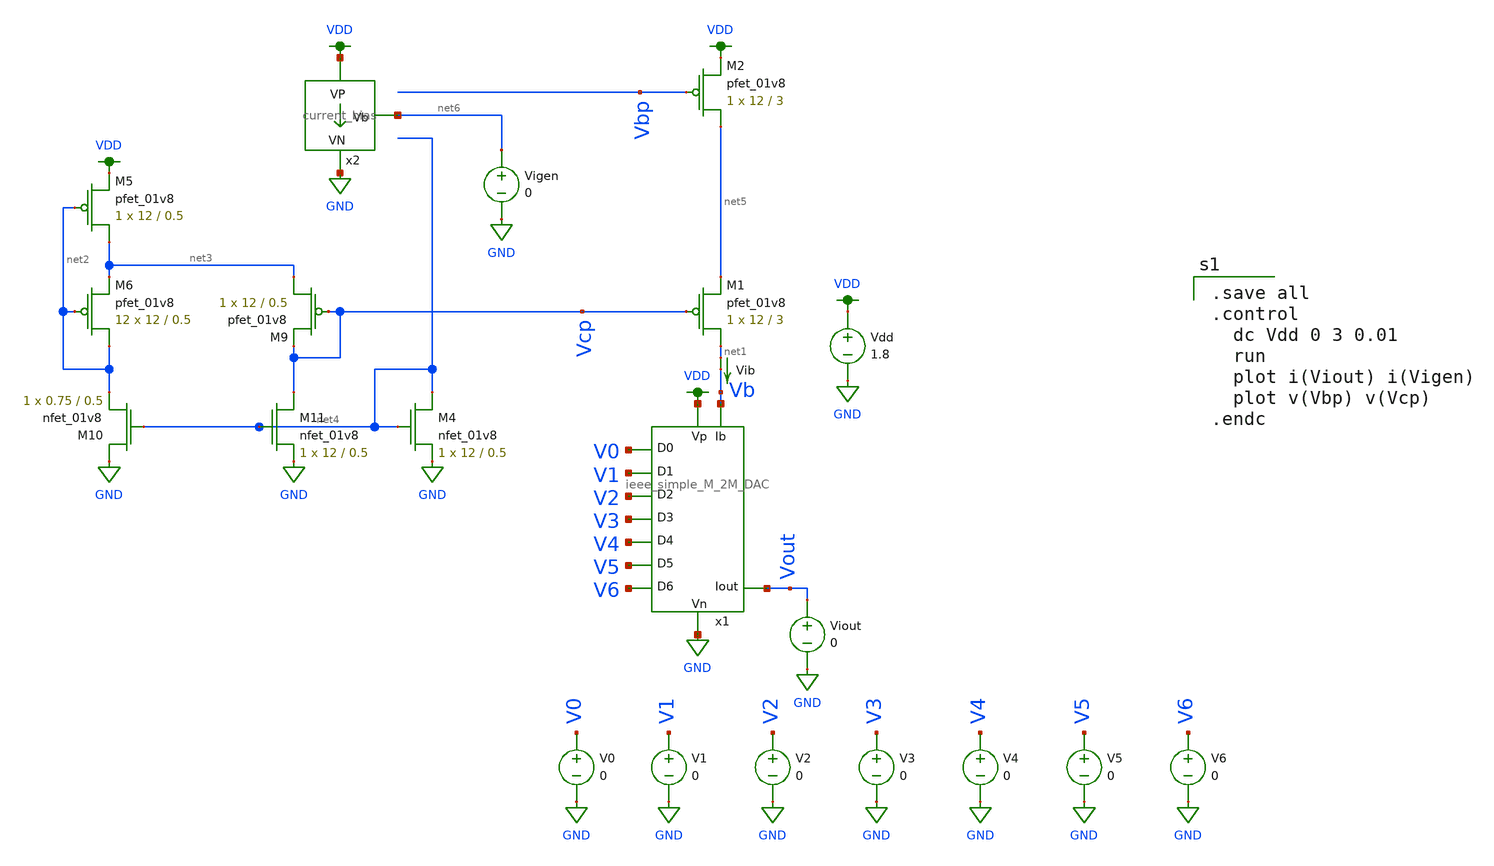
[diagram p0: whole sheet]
** sch_path: schematics/ieee DAC/characterization/bias_gen_with_cascode_and_vcn_generator.sch
**.subckt bias_gen_with_cascode_and_vcn_generator
Vdd VDD GND 1.8
V1 V1 GND 0
V2 V2 GND 0
V3 V3 GND 0
V4 V4 GND 0
V5 V5 GND 0
V6 V6 GND 0
V0 V0 GND 0
Viout Vout GND 0
Vib net1 Vb 0
.save i(vib)
x1 VDD Vout GND V1 V0 V2 V3 V4 V5 V6 Vb ieee_simple_M_2M_DAC
XM1 net1 Vcp net5 VDD sky130_fd_pr__pfet_01v8 L=3 W=12 nf=1 ad='int((nf+1)/2) * W/nf * 0.29' as='int((nf+2)/2) * W/nf * 0.29'
+ pd='2*int((nf+1)/2) * (W/nf + 0.29)' ps='2*int((nf+2)/2) * (W/nf + 0.29)' nrd='0.29 / W' nrs='0.29 / W'
+ sa=0 sb=0 sd=0 mult=1 m=1
XM5 net3 net2 VDD VDD sky130_fd_pr__pfet_01v8 L=0.5 W=12 nf=1 ad='int((nf+1)/2) * W/nf * 0.29' as='int((nf+2)/2) * W/nf * 0.29'
+ pd='2*int((nf+1)/2) * (W/nf + 0.29)' ps='2*int((nf+2)/2) * (W/nf + 0.29)' nrd='0.29 / W' nrs='0.29 / W'
+ sa=0 sb=0 sd=0 mult=1 m=1
XM6 net2 net2 net3 VDD sky130_fd_pr__pfet_01v8 L=0.5 W=12 nf=1 ad='int((nf+1)/2) * W/nf * 0.29' as='int((nf+2)/2) * W/nf * 0.29'
+ pd='2*int((nf+1)/2) * (W/nf + 0.29)' ps='2*int((nf+2)/2) * (W/nf + 0.29)' nrd='0.29 / W' nrs='0.29 / W'
+ sa=0 sb=0 sd=0 mult=12 m=12
XM9 net3 Vcp Vcp VDD sky130_fd_pr__pfet_01v8 L=0.5 W=12 nf=1 ad='int((nf+1)/2) * W/nf * 0.29' as='int((nf+2)/2) * W/nf * 0.29'
+ pd='2*int((nf+1)/2) * (W/nf + 0.29)' ps='2*int((nf+2)/2) * (W/nf + 0.29)' nrd='0.29 / W' nrs='0.29 / W'
+ sa=0 sb=0 sd=0 mult=1 m=1
XM10 GND net4 net2 GND sky130_fd_pr__nfet_01v8 L=0.5 W=0.75 nf=1 ad='int((nf+1)/2) * W/nf * 0.29' as='int((nf+2)/2) * W/nf * 0.29'
+ pd='2*int((nf+1)/2) * (W/nf + 0.29)' ps='2*int((nf+2)/2) * (W/nf + 0.29)' nrd='0.29 / W' nrs='0.29 / W'
+ sa=0 sb=0 sd=0 mult=1 m=1
XM11 Vcp net4 GND GND sky130_fd_pr__nfet_01v8 L=0.5 W=12 nf=1 ad='int((nf+1)/2) * W/nf * 0.29' as='int((nf+2)/2) * W/nf * 0.29'
+ pd='2*int((nf+1)/2) * (W/nf + 0.29)' ps='2*int((nf+2)/2) * (W/nf + 0.29)' nrd='0.29 / W' nrs='0.29 / W'
+ sa=0 sb=0 sd=0 mult=1 m=1
XM2 net5 Vbp VDD VDD sky130_fd_pr__pfet_01v8 L=3 W=12 nf=1 ad='int((nf+1)/2) * W/nf * 0.29' as='int((nf+2)/2) * W/nf * 0.29'
+ pd='2*int((nf+1)/2) * (W/nf + 0.29)' ps='2*int((nf+2)/2) * (W/nf + 0.29)' nrd='0.29 / W' nrs='0.29 / W'
+ sa=0 sb=0 sd=0 mult=1 m=1
XM4 net4 net4 GND GND sky130_fd_pr__nfet_01v8 L=0.5 W=12 nf=1 ad='int((nf+1)/2) * W/nf * 0.29' as='int((nf+2)/2) * W/nf * 0.29'
+ pd='2*int((nf+1)/2) * (W/nf + 0.29)' ps='2*int((nf+2)/2) * (W/nf + 0.29)' nrd='0.29 / W' nrs='0.29 / W'
+ sa=0 sb=0 sd=0 mult=1 m=1
x2 VDD net6 GND current_bias
Vigen net6 GND 0
**** begin user architecture code

.option wnflag=1
.param MC_SWITCH=1.0
.lib ~/skywater/skywater-pdk/libraries/sky130_fd_pr_ngspice/latest/models/sky130.lib.spice tt


.save all
.control
  dc Vdd 0 3 0.01
  run
  plot i(Viout) i(Vigen)
  plot v(Vbp) v(Vcp)
.endc

**** end user architecture code
**.ends
.GLOBAL VDD
.GLOBAL GND
.end
